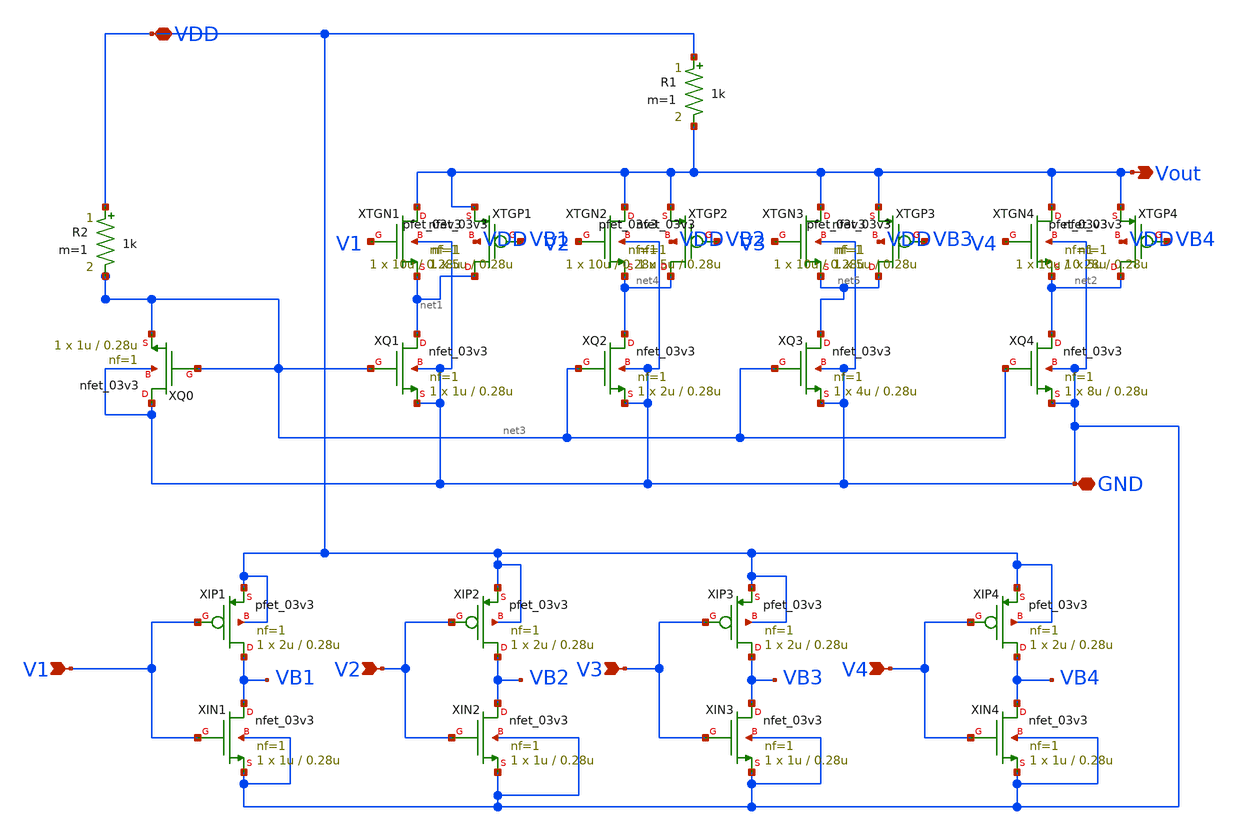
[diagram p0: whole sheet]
** sch_path: src/schematic/DAC/dac.sch
**.subckt dac V1 V2 V3 V4 Vout VDD GND
*.ipin V1
*.ipin V2
*.ipin V3
*.ipin V4
*.opin Vout
*.iopin VDD
*.iopin GND
R1 VDD Vout 1k m=1
R2 VDD net3 1k m=1
XQ1 net1 net3 GND GND nfet_03v3 L=0.28u W=1u nf=1 ad='int((nf+1)/2) * W/nf * 0.18u' as='int((nf+2)/2) * W/nf * 0.18u'
+ pd='2*int((nf+1)/2) * (W/nf + 0.18u)' ps='2*int((nf+2)/2) * (W/nf + 0.18u)' nrd='0.18u / W' nrs='0.18u / W'
+ sa=0 sb=0 sd=0 m=1
XQ2 net4 net3 GND GND nfet_03v3 L=0.28u W=2u nf=1 ad='int((nf+1)/2) * W/nf * 0.18u' as='int((nf+2)/2) * W/nf * 0.18u'
+ pd='2*int((nf+1)/2) * (W/nf + 0.18u)' ps='2*int((nf+2)/2) * (W/nf + 0.18u)' nrd='0.18u / W' nrs='0.18u / W'
+ sa=0 sb=0 sd=0 m=1
XQ3 net5 net3 GND GND nfet_03v3 L=0.28u W=4u nf=1 ad='int((nf+1)/2) * W/nf * 0.18u' as='int((nf+2)/2) * W/nf * 0.18u'
+ pd='2*int((nf+1)/2) * (W/nf + 0.18u)' ps='2*int((nf+2)/2) * (W/nf + 0.18u)' nrd='0.18u / W' nrs='0.18u / W'
+ sa=0 sb=0 sd=0 m=1
XQ4 net2 net3 GND GND nfet_03v3 L=0.28u W=8u nf=1 ad='int((nf+1)/2) * W/nf * 0.18u' as='int((nf+2)/2) * W/nf * 0.18u'
+ pd='2*int((nf+1)/2) * (W/nf + 0.18u)' ps='2*int((nf+2)/2) * (W/nf + 0.18u)' nrd='0.18u / W' nrs='0.18u / W'
+ sa=0 sb=0 sd=0 m=1
XQ0 GND net3 net3 GND nfet_03v3 L=0.28u W=1u nf=1 ad='int((nf+1)/2) * W/nf * 0.18u' as='int((nf+2)/2) * W/nf * 0.18u'
+ pd='2*int((nf+1)/2) * (W/nf + 0.18u)' ps='2*int((nf+2)/2) * (W/nf + 0.18u)' nrd='0.18u / W' nrs='0.18u / W'
+ sa=0 sb=0 sd=0 m=1
XTGN1 Vout V1 net1 GND nfet_03v3 L=0.28u W=5u nf=1 ad='int((nf+1)/2) * W/nf * 0.18u' as='int((nf+2)/2) * W/nf * 0.18u'
+ pd='2*int((nf+1)/2) * (W/nf + 0.18u)' ps='2*int((nf+2)/2) * (W/nf + 0.18u)' nrd='0.18u / W' nrs='0.18u / W'
+ sa=0 sb=0 sd=0 m=1
XTGN2 Vout V2 net4 GND nfet_03v3 L=0.28u W=5u nf=1 ad='int((nf+1)/2) * W/nf * 0.18u' as='int((nf+2)/2) * W/nf * 0.18u'
+ pd='2*int((nf+1)/2) * (W/nf + 0.18u)' ps='2*int((nf+2)/2) * (W/nf + 0.18u)' nrd='0.18u / W' nrs='0.18u / W'
+ sa=0 sb=0 sd=0 m=1
XTGN3 Vout V3 net5 GND nfet_03v3 L=0.28u W=5u nf=1 ad='int((nf+1)/2) * W/nf * 0.18u' as='int((nf+2)/2) * W/nf * 0.18u'
+ pd='2*int((nf+1)/2) * (W/nf + 0.18u)' ps='2*int((nf+2)/2) * (W/nf + 0.18u)' nrd='0.18u / W' nrs='0.18u / W'
+ sa=0 sb=0 sd=0 m=1
XTGN4 Vout V4 net2 GND nfet_03v3 L=0.28u W=5u nf=1 ad='int((nf+1)/2) * W/nf * 0.18u' as='int((nf+2)/2) * W/nf * 0.18u'
+ pd='2*int((nf+1)/2) * (W/nf + 0.18u)' ps='2*int((nf+2)/2) * (W/nf + 0.18u)' nrd='0.18u / W' nrs='0.18u / W'
+ sa=0 sb=0 sd=0 m=1
XTGP1 net1 VB1 Vout VDD pfet_03v3 L=0.28u W=10u nf=1 ad='int((nf+1)/2) * W/nf * 0.18u' as='int((nf+2)/2) * W/nf * 0.18u'
+ pd='2*int((nf+1)/2) * (W/nf + 0.18u)' ps='2*int((nf+2)/2) * (W/nf + 0.18u)' nrd='0.18u / W' nrs='0.18u / W'
+ sa=0 sb=0 sd=0 m=1
XIN1 VB1 V1 GND GND nfet_03v3 L=0.28u W=1u nf=1 ad='int((nf+1)/2) * W/nf * 0.18u' as='int((nf+2)/2) * W/nf * 0.18u'
+ pd='2*int((nf+1)/2) * (W/nf + 0.18u)' ps='2*int((nf+2)/2) * (W/nf + 0.18u)' nrd='0.18u / W' nrs='0.18u / W'
+ sa=0 sb=0 sd=0 m=1
XIP1 VB1 V1 VDD VDD pfet_03v3 L=0.28u W=2u nf=1 ad='int((nf+1)/2) * W/nf * 0.18u' as='int((nf+2)/2) * W/nf * 0.18u'
+ pd='2*int((nf+1)/2) * (W/nf + 0.18u)' ps='2*int((nf+2)/2) * (W/nf + 0.18u)' nrd='0.18u / W' nrs='0.18u / W'
+ sa=0 sb=0 sd=0 m=1
XIN2 VB2 V2 GND GND nfet_03v3 L=0.28u W=1u nf=1 ad='int((nf+1)/2) * W/nf * 0.18u' as='int((nf+2)/2) * W/nf * 0.18u'
+ pd='2*int((nf+1)/2) * (W/nf + 0.18u)' ps='2*int((nf+2)/2) * (W/nf + 0.18u)' nrd='0.18u / W' nrs='0.18u / W'
+ sa=0 sb=0 sd=0 m=1
XIP2 VB2 V2 VDD VDD pfet_03v3 L=0.28u W=2u nf=1 ad='int((nf+1)/2) * W/nf * 0.18u' as='int((nf+2)/2) * W/nf * 0.18u'
+ pd='2*int((nf+1)/2) * (W/nf + 0.18u)' ps='2*int((nf+2)/2) * (W/nf + 0.18u)' nrd='0.18u / W' nrs='0.18u / W'
+ sa=0 sb=0 sd=0 m=1
XIN3 VB3 V3 GND GND nfet_03v3 L=0.28u W=1u nf=1 ad='int((nf+1)/2) * W/nf * 0.18u' as='int((nf+2)/2) * W/nf * 0.18u'
+ pd='2*int((nf+1)/2) * (W/nf + 0.18u)' ps='2*int((nf+2)/2) * (W/nf + 0.18u)' nrd='0.18u / W' nrs='0.18u / W'
+ sa=0 sb=0 sd=0 m=1
XIP3 VB3 V3 VDD VDD pfet_03v3 L=0.28u W=2u nf=1 ad='int((nf+1)/2) * W/nf * 0.18u' as='int((nf+2)/2) * W/nf * 0.18u'
+ pd='2*int((nf+1)/2) * (W/nf + 0.18u)' ps='2*int((nf+2)/2) * (W/nf + 0.18u)' nrd='0.18u / W' nrs='0.18u / W'
+ sa=0 sb=0 sd=0 m=1
XIN4 VB4 V4 GND GND nfet_03v3 L=0.28u W=1u nf=1 ad='int((nf+1)/2) * W/nf * 0.18u' as='int((nf+2)/2) * W/nf * 0.18u'
+ pd='2*int((nf+1)/2) * (W/nf + 0.18u)' ps='2*int((nf+2)/2) * (W/nf + 0.18u)' nrd='0.18u / W' nrs='0.18u / W'
+ sa=0 sb=0 sd=0 m=1
XIP4 VB4 V4 VDD VDD pfet_03v3 L=0.28u W=2u nf=1 ad='int((nf+1)/2) * W/nf * 0.18u' as='int((nf+2)/2) * W/nf * 0.18u'
+ pd='2*int((nf+1)/2) * (W/nf + 0.18u)' ps='2*int((nf+2)/2) * (W/nf + 0.18u)' nrd='0.18u / W' nrs='0.18u / W'
+ sa=0 sb=0 sd=0 m=1
XTGP2 net4 VB2 Vout VDD pfet_03v3 L=0.28u W=10u nf=1 ad='int((nf+1)/2) * W/nf * 0.18u' as='int((nf+2)/2) * W/nf * 0.18u'
+ pd='2*int((nf+1)/2) * (W/nf + 0.18u)' ps='2*int((nf+2)/2) * (W/nf + 0.18u)' nrd='0.18u / W' nrs='0.18u / W'
+ sa=0 sb=0 sd=0 m=1
XTGP3 net5 VB3 Vout VDD pfet_03v3 L=0.28u W=10u nf=1 ad='int((nf+1)/2) * W/nf * 0.18u' as='int((nf+2)/2) * W/nf * 0.18u'
+ pd='2*int((nf+1)/2) * (W/nf + 0.18u)' ps='2*int((nf+2)/2) * (W/nf + 0.18u)' nrd='0.18u / W' nrs='0.18u / W'
+ sa=0 sb=0 sd=0 m=1
XTGP4 net2 VB4 Vout VDD pfet_03v3 L=0.28u W=10u nf=1 ad='int((nf+1)/2) * W/nf * 0.18u' as='int((nf+2)/2) * W/nf * 0.18u'
+ pd='2*int((nf+1)/2) * (W/nf + 0.18u)' ps='2*int((nf+2)/2) * (W/nf + 0.18u)' nrd='0.18u / W' nrs='0.18u / W'
+ sa=0 sb=0 sd=0 m=1
**.ends
.end
